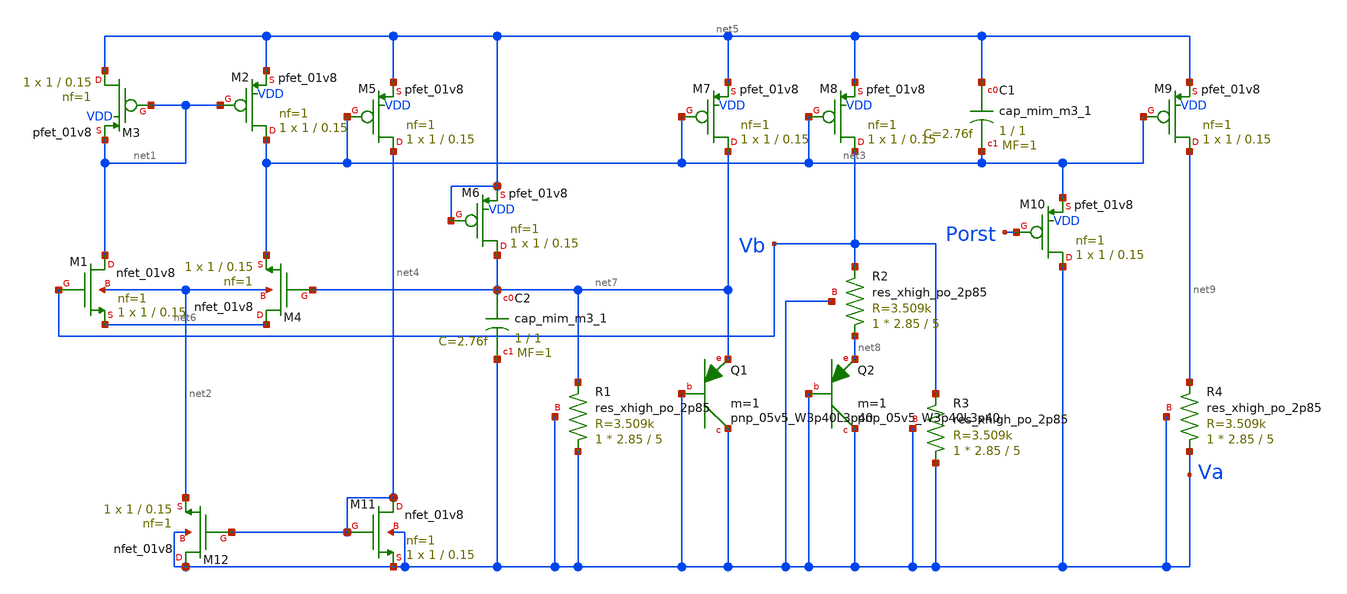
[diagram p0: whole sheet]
** sch_path: bgr.sch
**.subckt bgr
XM1 net1 Vb net6 net2 sky130_fd_pr__nfet_01v8 L=0.15 W=1 nf=1 ad='int((nf+1)/2) * W/nf * 0.29' as='int((nf+2)/2) * W/nf * 0.29'
+ pd='2*int((nf+1)/2) * (W/nf + 0.29)' ps='2*int((nf+2)/2) * (W/nf + 0.29)' nrd='0.29 / W' nrs='0.29 / W'
+ sa=0 sb=0 sd=0 mult=1 m=1
XM2 net3 net1 net5 VDD sky130_fd_pr__pfet_01v8 L=0.15 W=1 nf=1 ad='int((nf+1)/2) * W/nf * 0.29' as='int((nf+2)/2) * W/nf * 0.29'
+ pd='2*int((nf+1)/2) * (W/nf + 0.29)' ps='2*int((nf+2)/2) * (W/nf + 0.29)' nrd='0.29 / W' nrs='0.29 / W'
+ sa=0 sb=0 sd=0 mult=1 m=1
XM3 net5 net1 net1 VDD sky130_fd_pr__pfet_01v8 L=0.15 W=1 nf=1 ad='int((nf+1)/2) * W/nf * 0.29' as='int((nf+2)/2) * W/nf * 0.29'
+ pd='2*int((nf+1)/2) * (W/nf + 0.29)' ps='2*int((nf+2)/2) * (W/nf + 0.29)' nrd='0.29 / W' nrs='0.29 / W'
+ sa=0 sb=0 sd=0 mult=1 m=1
XM4 net6 net7 net3 net2 sky130_fd_pr__nfet_01v8 L=0.15 W=1 nf=1 ad='int((nf+1)/2) * W/nf * 0.29' as='int((nf+2)/2) * W/nf * 0.29'
+ pd='2*int((nf+1)/2) * (W/nf + 0.29)' ps='2*int((nf+2)/2) * (W/nf + 0.29)' nrd='0.29 / W' nrs='0.29 / W'
+ sa=0 sb=0 sd=0 mult=1 m=1
XM5 net4 net3 net5 VDD sky130_fd_pr__pfet_01v8 L=0.15 W=1 nf=1 ad='int((nf+1)/2) * W/nf * 0.29' as='int((nf+2)/2) * W/nf * 0.29'
+ pd='2*int((nf+1)/2) * (W/nf + 0.29)' ps='2*int((nf+2)/2) * (W/nf + 0.29)' nrd='0.29 / W' nrs='0.29 / W'
+ sa=0 sb=0 sd=0 mult=1 m=1
XM6 net7 net5 net5 VDD sky130_fd_pr__pfet_01v8 L=0.15 W=1 nf=1 ad='int((nf+1)/2) * W/nf * 0.29' as='int((nf+2)/2) * W/nf * 0.29'
+ pd='2*int((nf+1)/2) * (W/nf + 0.29)' ps='2*int((nf+2)/2) * (W/nf + 0.29)' nrd='0.29 / W' nrs='0.29 / W'
+ sa=0 sb=0 sd=0 mult=1 m=1
XM7 net7 net3 net5 VDD sky130_fd_pr__pfet_01v8 L=0.15 W=1 nf=1 ad='int((nf+1)/2) * W/nf * 0.29' as='int((nf+2)/2) * W/nf * 0.29'
+ pd='2*int((nf+1)/2) * (W/nf + 0.29)' ps='2*int((nf+2)/2) * (W/nf + 0.29)' nrd='0.29 / W' nrs='0.29 / W'
+ sa=0 sb=0 sd=0 mult=1 m=1
XM8 Vb net3 net5 VDD sky130_fd_pr__pfet_01v8 L=0.15 W=1 nf=1 ad='int((nf+1)/2) * W/nf * 0.29' as='int((nf+2)/2) * W/nf * 0.29'
+ pd='2*int((nf+1)/2) * (W/nf + 0.29)' ps='2*int((nf+2)/2) * (W/nf + 0.29)' nrd='0.29 / W' nrs='0.29 / W'
+ sa=0 sb=0 sd=0 mult=1 m=1
XM9 net9 net3 net5 VDD sky130_fd_pr__pfet_01v8 L=0.15 W=1 nf=1 ad='int((nf+1)/2) * W/nf * 0.29' as='int((nf+2)/2) * W/nf * 0.29'
+ pd='2*int((nf+1)/2) * (W/nf + 0.29)' ps='2*int((nf+2)/2) * (W/nf + 0.29)' nrd='0.29 / W' nrs='0.29 / W'
+ sa=0 sb=0 sd=0 mult=1 m=1
XC1 net5 net3 sky130_fd_pr__cap_mim_m3_1 W=1 L=1 MF=1 m=1
XM10 Va Porst net3 VDD sky130_fd_pr__pfet_01v8 L=0.15 W=1 nf=1 ad='int((nf+1)/2) * W/nf * 0.29' as='int((nf+2)/2) * W/nf * 0.29'
+ pd='2*int((nf+1)/2) * (W/nf + 0.29)' ps='2*int((nf+2)/2) * (W/nf + 0.29)' nrd='0.29 / W' nrs='0.29 / W'
+ sa=0 sb=0 sd=0 mult=1 m=1
XM11 net4 net4 Va Va sky130_fd_pr__nfet_01v8 L=0.15 W=1 nf=1 ad='int((nf+1)/2) * W/nf * 0.29' as='int((nf+2)/2) * W/nf * 0.29'
+ pd='2*int((nf+1)/2) * (W/nf + 0.29)' ps='2*int((nf+2)/2) * (W/nf + 0.29)' nrd='0.29 / W' nrs='0.29 / W'
+ sa=0 sb=0 sd=0 mult=1 m=1
XM12 Va net4 net2 Va sky130_fd_pr__nfet_01v8 L=0.15 W=1 nf=1 ad='int((nf+1)/2) * W/nf * 0.29' as='int((nf+2)/2) * W/nf * 0.29'
+ pd='2*int((nf+1)/2) * (W/nf + 0.29)' ps='2*int((nf+2)/2) * (W/nf + 0.29)' nrd='0.29 / W' nrs='0.29 / W'
+ sa=0 sb=0 sd=0 mult=1 m=1
XC2 net7 Va sky130_fd_pr__cap_mim_m3_1 W=1 L=1 MF=1 m=1
XR1 Va net7 Va sky130_fd_pr__res_xhigh_po_2p85 L=5 mult=1 m=1
XQ1 Va Va net7 sky130_fd_pr__pnp_05v5_W3p40L3p40 m=1
XQ2 Va Va net8 sky130_fd_pr__pnp_05v5_W3p40L3p40 m=1
XR2 net8 Vb Va sky130_fd_pr__res_xhigh_po_2p85 L=5 mult=1 m=1
XR3 Va Vb Va sky130_fd_pr__res_xhigh_po_2p85 L=5 mult=1 m=1
XR4 Va net9 Va sky130_fd_pr__res_xhigh_po_2p85 L=5 mult=1 m=1
**.ends
.end
